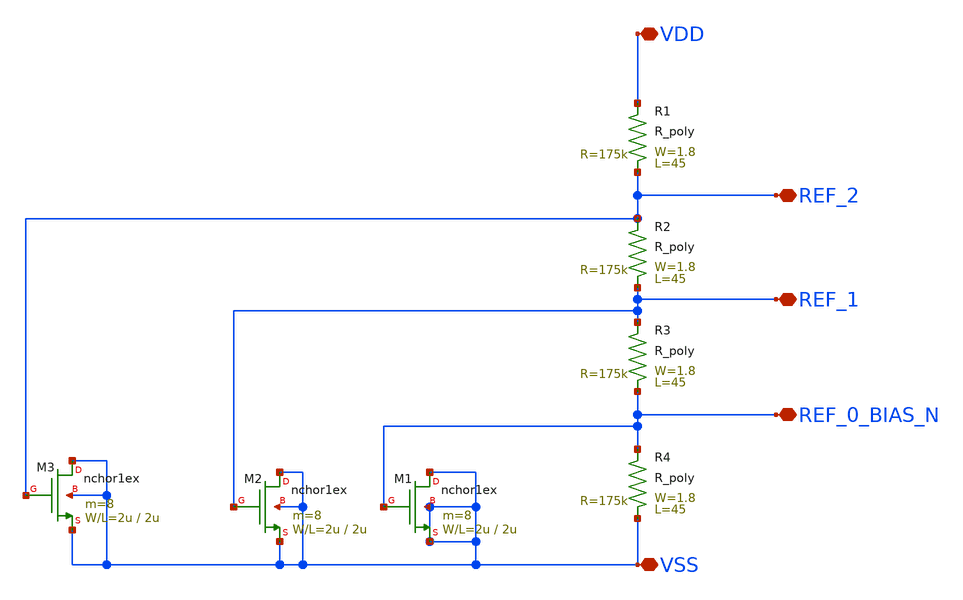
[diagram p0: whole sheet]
** sch_path: design/.design_bk/xschem/VCO/SA_DIV_VrefGen.sch
**.subckt SA_DIV_VrefGen VDD VSS REF_0_BIAS_N REF_1 REF_2
*.iopin VDD
*.iopin VSS
*.iopin REF_0_BIAS_N
*.iopin REF_1
*.iopin REF_2
M1 VSS REF_0_BIAS_N VSS VSS nchor1ex L=2u W=2u m=8
M2 VSS REF_1 VSS VSS nchor1ex L=2u W=2u m=8
M3 VSS REF_2 VSS VSS nchor1ex L=2u W=2u m=8
R1 REF_2 VDD R_poly W=1.8 L=45
R2 REF_1 REF_2 R_poly W=1.8 L=45
R3 REF_0_BIAS_N REF_1 R_poly W=1.8 L=45
R4 VSS REF_0_BIAS_N R_poly W=1.8 L=45
**.ends
.end
